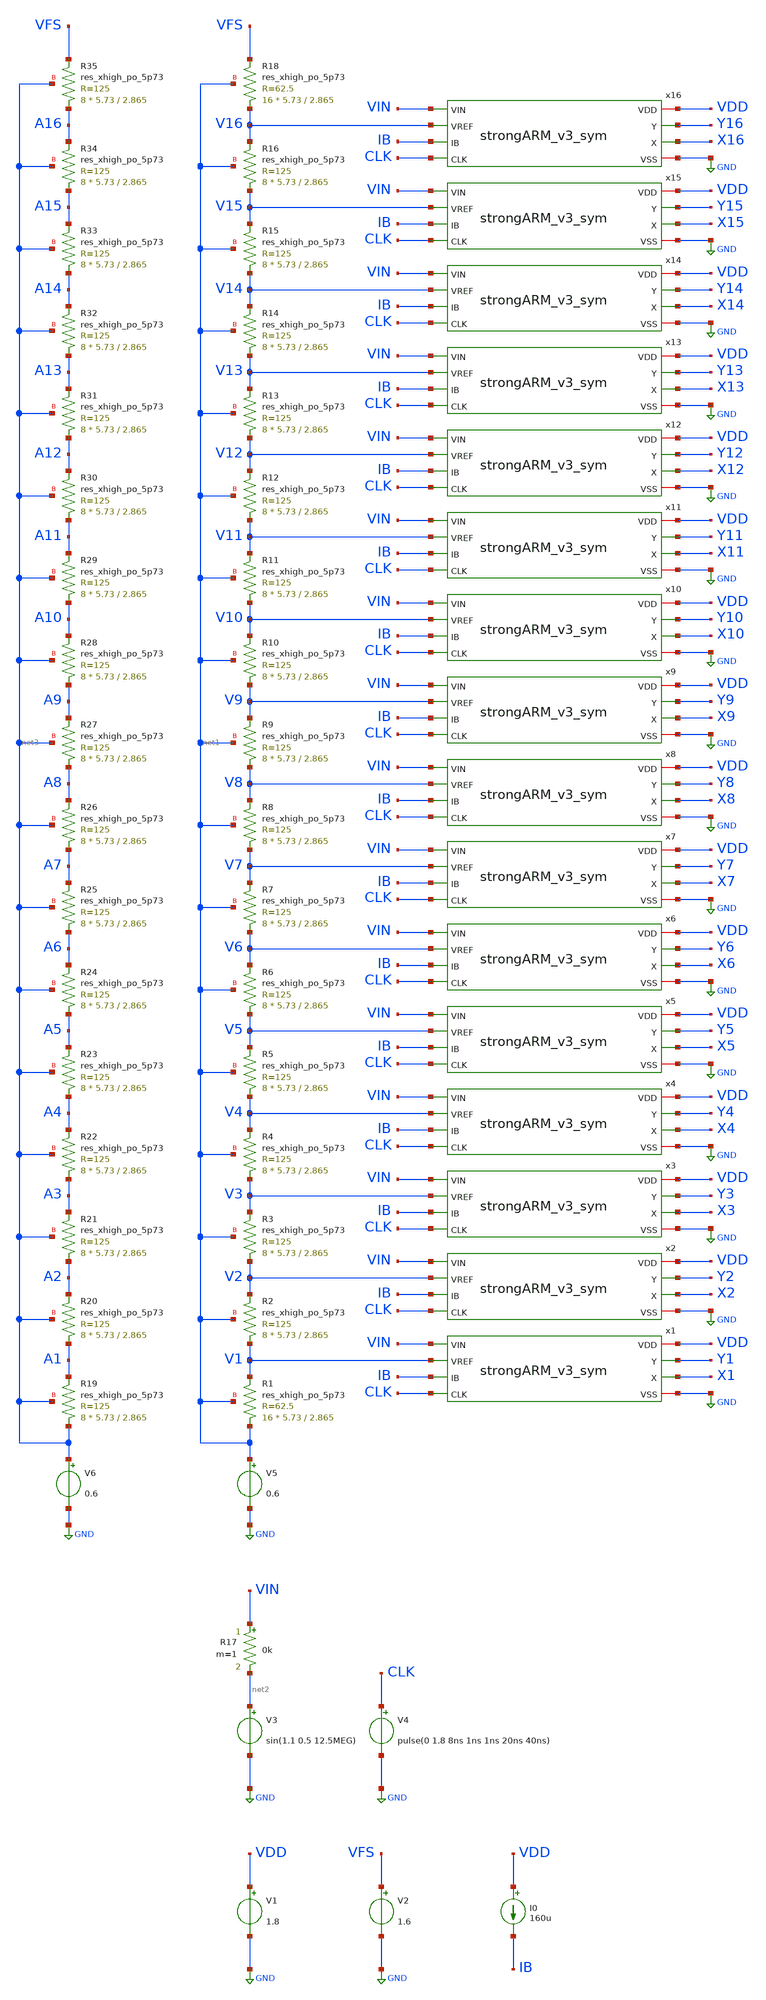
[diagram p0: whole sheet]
** sch_path: strongARM/flash_ADC_4b.sch
**.subckt flash_ADC_4b
x1 VDD Y1 X1 VIN V1 IB CLK GND strongARM_v3_sym
x2 VDD Y2 X2 VIN V2 IB CLK GND strongARM_v3_sym
V3 net2 GND sin(1.1 0.5 12.5MEG)
V4 CLK GND pulse(0 1.8 8ns 1ns 1ns 20ns 40ns)
V1 VDD GND 1.8
V2 VFS GND 1.6
R17 VIN net2 0k m=1
x3 VDD Y3 X3 VIN V3 IB CLK GND strongARM_v3_sym
x4 VDD Y4 X4 VIN V4 IB CLK GND strongARM_v3_sym
x5 VDD Y5 X5 VIN V5 IB CLK GND strongARM_v3_sym
x6 VDD Y6 X6 VIN V6 IB CLK GND strongARM_v3_sym
x7 VDD Y7 X7 VIN V7 IB CLK GND strongARM_v3_sym
x8 VDD Y8 X8 VIN V8 IB CLK GND strongARM_v3_sym
x9 VDD Y9 X9 VIN V9 IB CLK GND strongARM_v3_sym
x10 VDD Y10 X10 VIN V10 IB CLK GND strongARM_v3_sym
x11 VDD Y11 X11 VIN V11 IB CLK GND strongARM_v3_sym
x12 VDD Y12 X12 VIN V12 IB CLK GND strongARM_v3_sym
x13 VDD Y13 X13 VIN V13 IB CLK GND strongARM_v3_sym
x14 VDD Y14 X14 VIN V14 IB CLK GND strongARM_v3_sym
x15 VDD Y15 X15 VIN V15 IB CLK GND strongARM_v3_sym
x16 VDD Y16 X16 VIN V16 IB CLK GND strongARM_v3_sym
I0 VDD IB 160u
V5 net1 GND 0.6
XR19 net3 A1 net3 sky130_fd_pr__res_xhigh_po_5p73 L=2.865 mult=8 m=8
V6 net3 GND 0.6
XR20 A1 A2 net3 sky130_fd_pr__res_xhigh_po_5p73 L=2.865 mult=8 m=8
XR21 A2 A3 net3 sky130_fd_pr__res_xhigh_po_5p73 L=2.865 mult=8 m=8
XR22 A3 A4 net3 sky130_fd_pr__res_xhigh_po_5p73 L=2.865 mult=8 m=8
XR23 A4 A5 net3 sky130_fd_pr__res_xhigh_po_5p73 L=2.865 mult=8 m=8
XR24 A5 A6 net3 sky130_fd_pr__res_xhigh_po_5p73 L=2.865 mult=8 m=8
XR25 A6 A7 net3 sky130_fd_pr__res_xhigh_po_5p73 L=2.865 mult=8 m=8
XR26 A7 A8 net3 sky130_fd_pr__res_xhigh_po_5p73 L=2.865 mult=8 m=8
XR27 A8 A9 net3 sky130_fd_pr__res_xhigh_po_5p73 L=2.865 mult=8 m=8
XR28 A9 A10 net3 sky130_fd_pr__res_xhigh_po_5p73 L=2.865 mult=8 m=8
XR29 A10 A11 net3 sky130_fd_pr__res_xhigh_po_5p73 L=2.865 mult=8 m=8
XR30 A11 A12 net3 sky130_fd_pr__res_xhigh_po_5p73 L=2.865 mult=8 m=8
XR31 A12 A13 net3 sky130_fd_pr__res_xhigh_po_5p73 L=2.865 mult=8 m=8
XR32 A13 A14 net3 sky130_fd_pr__res_xhigh_po_5p73 L=2.865 mult=8 m=8
XR33 A14 A15 net3 sky130_fd_pr__res_xhigh_po_5p73 L=2.865 mult=8 m=8
XR34 A15 A16 net3 sky130_fd_pr__res_xhigh_po_5p73 L=2.865 mult=8 m=8
XR35 A16 VFS net3 sky130_fd_pr__res_xhigh_po_5p73 L=2.865 mult=8 m=8
XR1 net1 V1 net1 sky130_fd_pr__res_xhigh_po_5p73 L=2.865 mult=16 m=16
XR2 V1 V2 net1 sky130_fd_pr__res_xhigh_po_5p73 L=2.865 mult=8 m=8
XR3 V2 V3 net1 sky130_fd_pr__res_xhigh_po_5p73 L=2.865 mult=8 m=8
XR4 V3 V4 net1 sky130_fd_pr__res_xhigh_po_5p73 L=2.865 mult=8 m=8
XR5 V4 V5 net1 sky130_fd_pr__res_xhigh_po_5p73 L=2.865 mult=8 m=8
XR6 V5 V6 net1 sky130_fd_pr__res_xhigh_po_5p73 L=2.865 mult=8 m=8
XR7 V6 V7 net1 sky130_fd_pr__res_xhigh_po_5p73 L=2.865 mult=8 m=8
XR8 V7 V8 net1 sky130_fd_pr__res_xhigh_po_5p73 L=2.865 mult=8 m=8
XR9 V8 V9 net1 sky130_fd_pr__res_xhigh_po_5p73 L=2.865 mult=8 m=8
XR10 V9 V10 net1 sky130_fd_pr__res_xhigh_po_5p73 L=2.865 mult=8 m=8
XR11 V10 V11 net1 sky130_fd_pr__res_xhigh_po_5p73 L=2.865 mult=8 m=8
XR12 V11 V12 net1 sky130_fd_pr__res_xhigh_po_5p73 L=2.865 mult=8 m=8
XR13 V12 V13 net1 sky130_fd_pr__res_xhigh_po_5p73 L=2.865 mult=8 m=8
XR14 V13 V14 net1 sky130_fd_pr__res_xhigh_po_5p73 L=2.865 mult=8 m=8
XR15 V14 V15 net1 sky130_fd_pr__res_xhigh_po_5p73 L=2.865 mult=8 m=8
XR16 V15 V16 net1 sky130_fd_pr__res_xhigh_po_5p73 L=2.865 mult=8 m=8
XR18 V16 VFS net1 sky130_fd_pr__res_xhigh_po_5p73 L=2.865 mult=16 m=16
**** begin user architecture code
.lib $::SKYWATER_MODELS/sky130.lib.spice tt


.options savecurrents
.control

save all

tran 0.005n 240n
remzerovec
write flash_ADC_4b.raw

.endc


**** end user architecture code
**.ends

* expanding   symbol:  /foss/designs/Analog_FA23_SP24/strongARM/strongARM_v3_sym.sym # of pins=8
** sym_path: strongARM/strongARM_v3_sym.sym
** sch_path: strongARM/strongARM_v3_sym.sch
.subckt strongARM_v3_sym VDD Y X VIN VREF IB CLK VSS
*.ipin IB
*.ipin CLK
*.iopin VSS
*.iopin VDD
*.opin Y
*.opin X
*.ipin VIN
*.ipin VREF
XM2 P VOUTN net1 VSS sky130_fd_pr__nfet_01v8_lvt L=0.15 W=4 nf=1 ad='int((nf+1)/2) * W/nf * 0.29' as='int((nf+2)/2) * W/nf * 0.29'
+ pd='2*int((nf+1)/2) * (W/nf + 0.29)' ps='2*int((nf+2)/2) * (W/nf + 0.29)' nrd='0.29 / W' nrs='0.29 / W'
+ sa=0 sb=0 sd=0 mult=6 m=6
XM3 Q VOUTP net1 VSS sky130_fd_pr__nfet_01v8_lvt L=0.15 W=4 nf=1 ad='int((nf+1)/2) * W/nf * 0.29' as='int((nf+2)/2) * W/nf * 0.29'
+ pd='2*int((nf+1)/2) * (W/nf + 0.29)' ps='2*int((nf+2)/2) * (W/nf + 0.29)' nrd='0.29 / W' nrs='0.29 / W'
+ sa=0 sb=0 sd=0 mult=6 m=6
XM4 P CLK VDD VDD sky130_fd_pr__pfet_01v8_lvt L=0.35 W=1 nf=1 ad='int((nf+1)/2) * W/nf * 0.29' as='int((nf+2)/2) * W/nf * 0.29'
+ pd='2*int((nf+1)/2) * (W/nf + 0.29)' ps='2*int((nf+2)/2) * (W/nf + 0.29)' nrd='0.29 / W' nrs='0.29 / W'
+ sa=0 sb=0 sd=0 mult=1 m=1
XM5 X CLK VDD VDD sky130_fd_pr__pfet_01v8_lvt L=0.35 W=1 nf=1 ad='int((nf+1)/2) * W/nf * 0.29' as='int((nf+2)/2) * W/nf * 0.29'
+ pd='2*int((nf+1)/2) * (W/nf + 0.29)' ps='2*int((nf+2)/2) * (W/nf + 0.29)' nrd='0.29 / W' nrs='0.29 / W'
+ sa=0 sb=0 sd=0 mult=1 m=1
XM6 Y X VDD VDD sky130_fd_pr__pfet_01v8_lvt L=0.35 W=1 nf=1 ad='int((nf+1)/2) * W/nf * 0.29' as='int((nf+2)/2) * W/nf * 0.29'
+ pd='2*int((nf+1)/2) * (W/nf + 0.29)' ps='2*int((nf+2)/2) * (W/nf + 0.29)' nrd='0.29 / W' nrs='0.29 / W'
+ sa=0 sb=0 sd=0 mult=1 m=1
XM7 X Y VDD VDD sky130_fd_pr__pfet_01v8_lvt L=0.35 W=1 nf=1 ad='int((nf+1)/2) * W/nf * 0.29' as='int((nf+2)/2) * W/nf * 0.29'
+ pd='2*int((nf+1)/2) * (W/nf + 0.29)' ps='2*int((nf+2)/2) * (W/nf + 0.29)' nrd='0.29 / W' nrs='0.29 / W'
+ sa=0 sb=0 sd=0 mult=1 m=1
XM8 Y CLK VDD VDD sky130_fd_pr__pfet_01v8_lvt L=0.35 W=1 nf=1 ad='int((nf+1)/2) * W/nf * 0.29' as='int((nf+2)/2) * W/nf * 0.29'
+ pd='2*int((nf+1)/2) * (W/nf + 0.29)' ps='2*int((nf+2)/2) * (W/nf + 0.29)' nrd='0.29 / W' nrs='0.29 / W'
+ sa=0 sb=0 sd=0 mult=1 m=1
XM9 Q CLK VDD VDD sky130_fd_pr__pfet_01v8_lvt L=0.35 W=1 nf=1 ad='int((nf+1)/2) * W/nf * 0.29' as='int((nf+2)/2) * W/nf * 0.29'
+ pd='2*int((nf+1)/2) * (W/nf + 0.29)' ps='2*int((nf+2)/2) * (W/nf + 0.29)' nrd='0.29 / W' nrs='0.29 / W'
+ sa=0 sb=0 sd=0 mult=1 m=1
XM10 X Y P VSS sky130_fd_pr__nfet_01v8_lvt L=0.15 W=1 nf=1 ad='int((nf+1)/2) * W/nf * 0.29' as='int((nf+2)/2) * W/nf * 0.29'
+ pd='2*int((nf+1)/2) * (W/nf + 0.29)' ps='2*int((nf+2)/2) * (W/nf + 0.29)' nrd='0.29 / W' nrs='0.29 / W'
+ sa=0 sb=0 sd=0 mult=1 m=1
XM11 Y X Q VSS sky130_fd_pr__nfet_01v8_lvt L=0.15 W=1 nf=1 ad='int((nf+1)/2) * W/nf * 0.29' as='int((nf+2)/2) * W/nf * 0.29'
+ pd='2*int((nf+1)/2) * (W/nf + 0.29)' ps='2*int((nf+2)/2) * (W/nf + 0.29)' nrd='0.29 / W' nrs='0.29 / W'
+ sa=0 sb=0 sd=0 mult=1 m=1
XM1 net1 CLK VSS VSS sky130_fd_pr__nfet_01v8_lvt L=0.15 W=4 nf=1 ad='int((nf+1)/2) * W/nf * 0.29' as='int((nf+2)/2) * W/nf * 0.29'
+ pd='2*int((nf+1)/2) * (W/nf + 0.29)' ps='2*int((nf+2)/2) * (W/nf + 0.29)' nrd='0.29 / W' nrs='0.29 / W'
+ sa=0 sb=0 sd=0 mult=1 m=1
XM12 IB IB VSS VSS sky130_fd_pr__nfet_01v8_lvt L=0.6 W=4 nf=1 ad='int((nf+1)/2) * W/nf * 0.29' as='int((nf+2)/2) * W/nf * 0.29'
+ pd='2*int((nf+1)/2) * (W/nf + 0.29)' ps='2*int((nf+2)/2) * (W/nf + 0.29)' nrd='0.29 / W' nrs='0.29 / W'
+ sa=0 sb=0 sd=0 mult=1 m=1
XM13 VIR IB VSS VSS sky130_fd_pr__nfet_01v8_lvt L=0.6 W=4 nf=1 ad='int((nf+1)/2) * W/nf * 0.29' as='int((nf+2)/2) * W/nf * 0.29'
+ pd='2*int((nf+1)/2) * (W/nf + 0.29)' ps='2*int((nf+2)/2) * (W/nf + 0.29)' nrd='0.29 / W' nrs='0.29 / W'
+ sa=0 sb=0 sd=0 mult=4 m=4
XM14 VOUTN VIN VIR VSS sky130_fd_pr__nfet_01v8_lvt L=0.6 W=4 nf=1 ad='int((nf+1)/2) * W/nf * 0.29' as='int((nf+2)/2) * W/nf * 0.29'
+ pd='2*int((nf+1)/2) * (W/nf + 0.29)' ps='2*int((nf+2)/2) * (W/nf + 0.29)' nrd='0.29 / W' nrs='0.29 / W'
+ sa=0 sb=0 sd=0 mult=2 m=2
XM15 VOUTP VREF VIR VSS sky130_fd_pr__nfet_01v8_lvt L=0.6 W=4 nf=1 ad='int((nf+1)/2) * W/nf * 0.29' as='int((nf+2)/2) * W/nf * 0.29'
+ pd='2*int((nf+1)/2) * (W/nf + 0.29)' ps='2*int((nf+2)/2) * (W/nf + 0.29)' nrd='0.29 / W' nrs='0.29 / W'
+ sa=0 sb=0 sd=0 mult=2 m=2
XM16 VOUTP VP_BIAS VDD VDD sky130_fd_pr__pfet_01v8_lvt L=1 W=19 nf=1 ad='int((nf+1)/2) * W/nf * 0.29'
+ as='int((nf+2)/2) * W/nf * 0.29' pd='2*int((nf+1)/2) * (W/nf + 0.29)' ps='2*int((nf+2)/2) * (W/nf + 0.29)'
+ nrd='0.29 / W' nrs='0.29 / W' sa=0 sb=0 sd=0 mult=2 m=2
XM17 VDD VOUTN net2 VSS sky130_fd_pr__nfet_01v8_lvt L=0.6 W=4 nf=1 ad='int((nf+1)/2) * W/nf * 0.29' as='int((nf+2)/2) * W/nf * 0.29'
+ pd='2*int((nf+1)/2) * (W/nf + 0.29)' ps='2*int((nf+2)/2) * (W/nf + 0.29)' nrd='0.29 / W' nrs='0.29 / W'
+ sa=0 sb=0 sd=0 mult=1 m=1
XM18 VP_BIAS net4 net2 VSS sky130_fd_pr__nfet_01v8_lvt L=0.6 W=4 nf=1 ad='int((nf+1)/2) * W/nf * 0.29'
+ as='int((nf+2)/2) * W/nf * 0.29' pd='2*int((nf+1)/2) * (W/nf + 0.29)' ps='2*int((nf+2)/2) * (W/nf + 0.29)'
+ nrd='0.29 / W' nrs='0.29 / W' sa=0 sb=0 sd=0 mult=1 m=1
XM19 VP_BIAS net4 net3 VSS sky130_fd_pr__nfet_01v8_lvt L=0.6 W=4 nf=1 ad='int((nf+1)/2) * W/nf * 0.29'
+ as='int((nf+2)/2) * W/nf * 0.29' pd='2*int((nf+1)/2) * (W/nf + 0.29)' ps='2*int((nf+2)/2) * (W/nf + 0.29)'
+ nrd='0.29 / W' nrs='0.29 / W' sa=0 sb=0 sd=0 mult=1 m=1
XM20 VDD VOUTP net3 VSS sky130_fd_pr__nfet_01v8_lvt L=0.6 W=4 nf=1 ad='int((nf+1)/2) * W/nf * 0.29' as='int((nf+2)/2) * W/nf * 0.29'
+ pd='2*int((nf+1)/2) * (W/nf + 0.29)' ps='2*int((nf+2)/2) * (W/nf + 0.29)' nrd='0.29 / W' nrs='0.29 / W'
+ sa=0 sb=0 sd=0 mult=1 m=1
XM21 net2 IB VSS VSS sky130_fd_pr__nfet_01v8_lvt L=0.6 W=4 nf=1 ad='int((nf+1)/2) * W/nf * 0.29' as='int((nf+2)/2) * W/nf * 0.29'
+ pd='2*int((nf+1)/2) * (W/nf + 0.29)' ps='2*int((nf+2)/2) * (W/nf + 0.29)' nrd='0.29 / W' nrs='0.29 / W'
+ sa=0 sb=0 sd=0 mult=2 m=2
XM22 net3 IB VSS VSS sky130_fd_pr__nfet_01v8_lvt L=0.6 W=4 nf=1 ad='int((nf+1)/2) * W/nf * 0.29' as='int((nf+2)/2) * W/nf * 0.29'
+ pd='2*int((nf+1)/2) * (W/nf + 0.29)' ps='2*int((nf+2)/2) * (W/nf + 0.29)' nrd='0.29 / W' nrs='0.29 / W'
+ sa=0 sb=0 sd=0 mult=2 m=2
XM23 VP_BIAS VP_BIAS VDD VDD sky130_fd_pr__pfet_01v8_lvt L=1 W=19 nf=1 ad='int((nf+1)/2) * W/nf * 0.29'
+ as='int((nf+2)/2) * W/nf * 0.29' pd='2*int((nf+1)/2) * (W/nf + 0.29)' ps='2*int((nf+2)/2) * (W/nf + 0.29)'
+ nrd='0.29 / W' nrs='0.29 / W' sa=0 sb=0 sd=0 mult=2 m=2
V6 net4 GND 0.9
XM24 VOUTN VP_BIAS VDD VDD sky130_fd_pr__pfet_01v8_lvt L=1 W=19 nf=1 ad='int((nf+1)/2) * W/nf * 0.29'
+ as='int((nf+2)/2) * W/nf * 0.29' pd='2*int((nf+1)/2) * (W/nf + 0.29)' ps='2*int((nf+2)/2) * (W/nf + 0.29)'
+ nrd='0.29 / W' nrs='0.29 / W' sa=0 sb=0 sd=0 mult=2 m=2
.ends

.GLOBAL GND
.end
